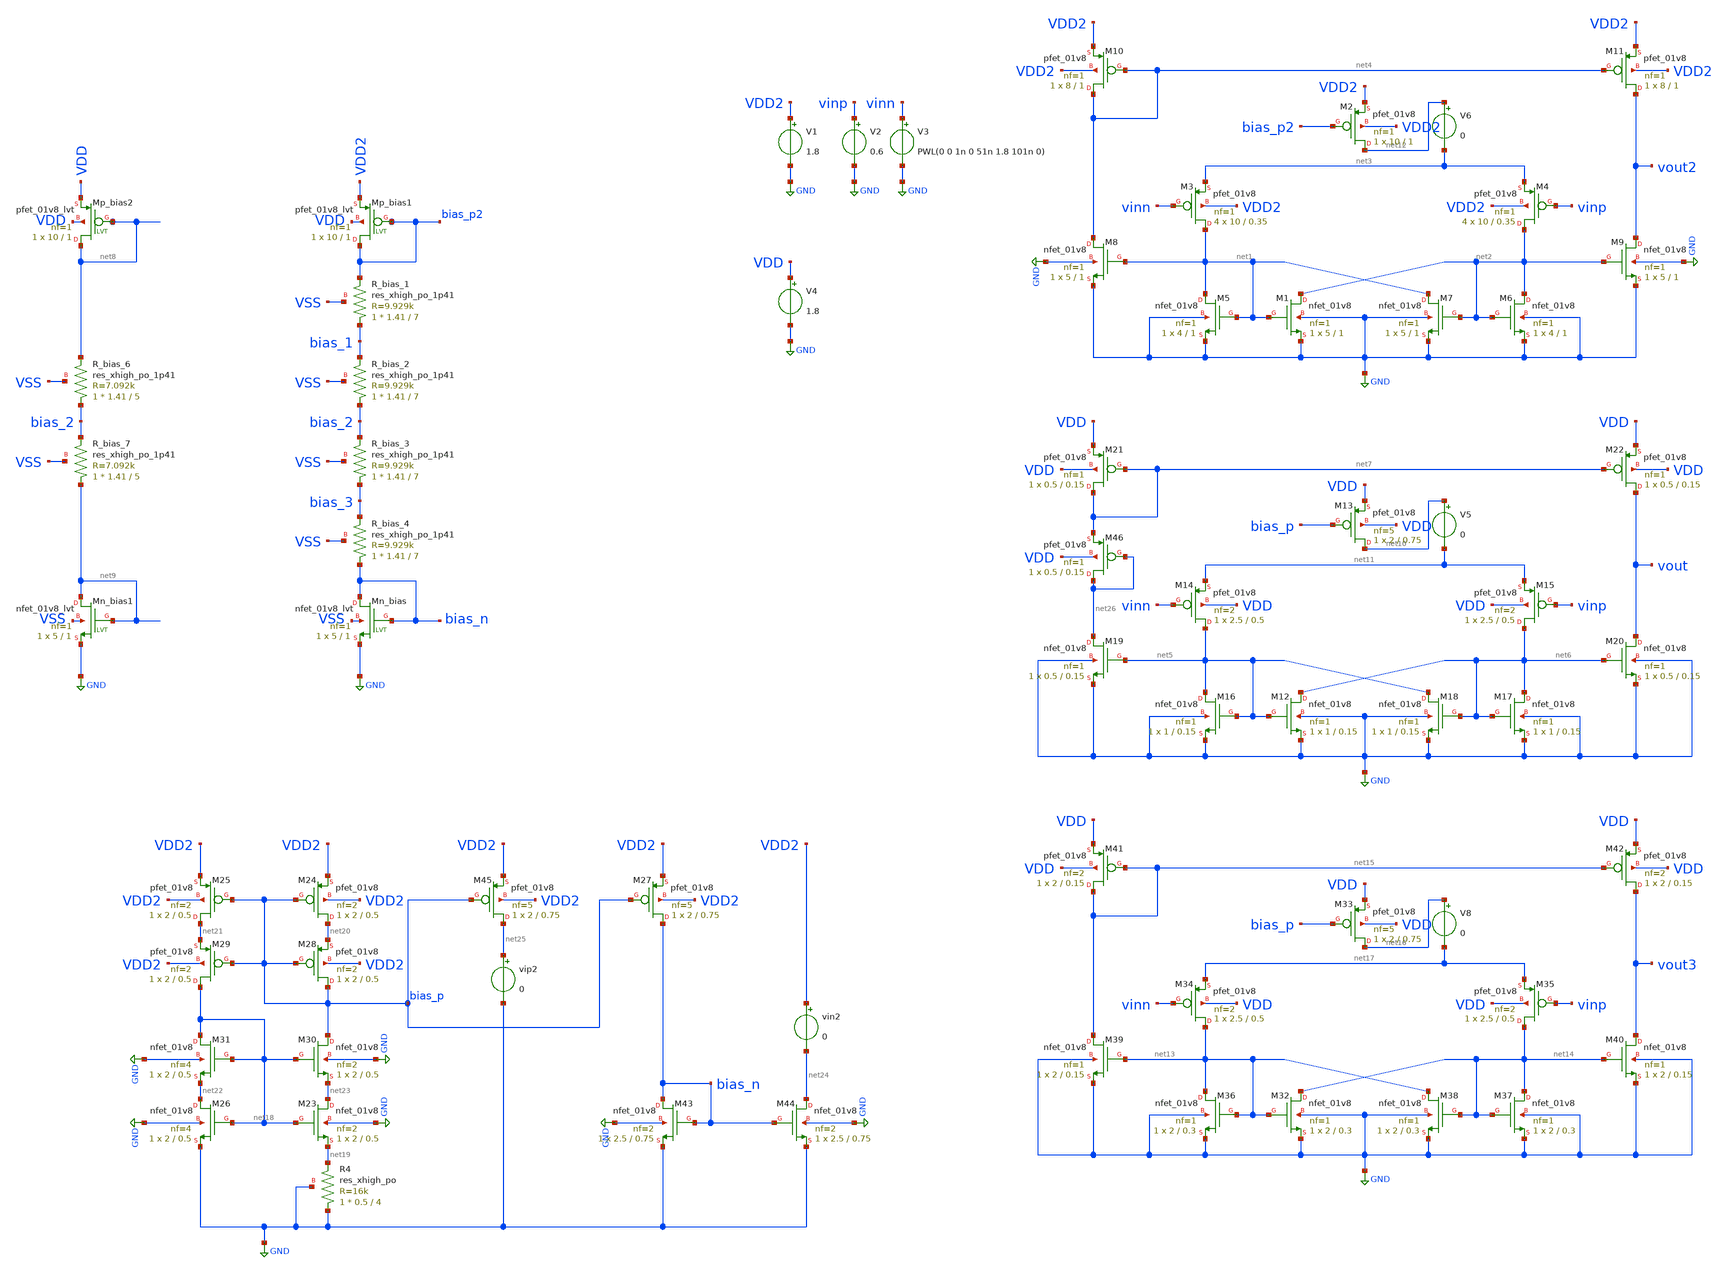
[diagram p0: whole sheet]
** sch_path: schem/comp_p.sch
**.subckt comp_p
XM1 net2 net1 GND GND sky130_fd_pr__nfet_01v8 L=1 W=5 nf=1 ad='int((1 + 1)/2) * 5 / 1 * 0.29' as='int((1 + 2)/2) * 5 / 1 * 0.29'
+ pd='2*int((1 + 1)/2) * (5 / 1 + 0.29)' ps='2*int((1 + 2)/2) * (5 / 1 + 0.29)' nrd='0.29 / 5 ' nrs='0.29 / 5 '
+ sa=0 sb=0 sd=0 mult=1 m=1
XM2 net12 bias_p2 VDD2 VDD2 sky130_fd_pr__pfet_01v8 L=1 W=10 nf=1 ad='int((1 + 1)/2) * 10 / 1 * 0.29'
+ as='int((1 + 2)/2) * 10 / 1 * 0.29' pd='2*int((1 + 1)/2) * (10 / 1 + 0.29)' ps='2*int((1 + 2)/2) * (10 / 1 + 0.29)'
+ nrd='0.29 / 10 ' nrs='0.29 / 10 ' sa=0 sb=0 sd=0 mult=1 m=1
XM3 net1 vinn net3 VDD2 sky130_fd_pr__pfet_01v8 L=0.35 W=10 nf=1 ad='int((1 + 1)/2) * 10 / 1 * 0.29'
+ as='int((1 + 2)/2) * 10 / 1 * 0.29' pd='2*int((1 + 1)/2) * (10 / 1 + 0.29)' ps='2*int((1 + 2)/2) * (10 / 1 + 0.29)'
+ nrd='0.29 / 10 ' nrs='0.29 / 10 ' sa=0 sb=0 sd=0 mult=4 m=4
XM4 net2 vinp net3 VDD2 sky130_fd_pr__pfet_01v8 L=0.35 W=10 nf=1 ad='int((1 + 1)/2) * 10 / 1 * 0.29'
+ as='int((1 + 2)/2) * 10 / 1 * 0.29' pd='2*int((1 + 1)/2) * (10 / 1 + 0.29)' ps='2*int((1 + 2)/2) * (10 / 1 + 0.29)'
+ nrd='0.29 / 10 ' nrs='0.29 / 10 ' sa=0 sb=0 sd=0 mult=4 m=4
XM5 net1 net1 GND GND sky130_fd_pr__nfet_01v8 L=1 W=4 nf=1 ad='int((1 + 1)/2) * 4 / 1 * 0.29' as='int((1 + 2)/2) * 4 / 1 * 0.29'
+ pd='2*int((1 + 1)/2) * (4 / 1 + 0.29)' ps='2*int((1 + 2)/2) * (4 / 1 + 0.29)' nrd='0.29 / 4 ' nrs='0.29 / 4 '
+ sa=0 sb=0 sd=0 mult=1 m=1
XM6 net2 net2 GND GND sky130_fd_pr__nfet_01v8 L=1 W=4 nf=1 ad='int((1 + 1)/2) * 4 / 1 * 0.29' as='int((1 + 2)/2) * 4 / 1 * 0.29'
+ pd='2*int((1 + 1)/2) * (4 / 1 + 0.29)' ps='2*int((1 + 2)/2) * (4 / 1 + 0.29)' nrd='0.29 / 4 ' nrs='0.29 / 4 '
+ sa=0 sb=0 sd=0 mult=1 m=1
XM7 net1 net2 GND GND sky130_fd_pr__nfet_01v8 L=1 W=5 nf=1 ad='int((1 + 1)/2) * 5 / 1 * 0.29' as='int((1 + 2)/2) * 5 / 1 * 0.29'
+ pd='2*int((1 + 1)/2) * (5 / 1 + 0.29)' ps='2*int((1 + 2)/2) * (5 / 1 + 0.29)' nrd='0.29 / 5 ' nrs='0.29 / 5 '
+ sa=0 sb=0 sd=0 mult=1 m=1
XM8 net4 net1 GND GND sky130_fd_pr__nfet_01v8 L=1 W=5 nf=1 ad='int((1 + 1)/2) * 5 / 1 * 0.29' as='int((1 + 2)/2) * 5 / 1 * 0.29'
+ pd='2*int((1 + 1)/2) * (5 / 1 + 0.29)' ps='2*int((1 + 2)/2) * (5 / 1 + 0.29)' nrd='0.29 / 5 ' nrs='0.29 / 5 '
+ sa=0 sb=0 sd=0 mult=1 m=1
XM9 vout2 net2 GND GND sky130_fd_pr__nfet_01v8 L=1 W=5 nf=1 ad='int((1 + 1)/2) * 5 / 1 * 0.29' as='int((1 + 2)/2) * 5 / 1 * 0.29'
+ pd='2*int((1 + 1)/2) * (5 / 1 + 0.29)' ps='2*int((1 + 2)/2) * (5 / 1 + 0.29)' nrd='0.29 / 5 ' nrs='0.29 / 5 '
+ sa=0 sb=0 sd=0 mult=1 m=1
XM10 net4 net4 VDD2 VDD2 sky130_fd_pr__pfet_01v8 L=1 W=8 nf=1 ad='int((1 + 1)/2) * 8 / 1 * 0.29' as='int((1 + 2)/2) * 8 / 1 * 0.29'
+ pd='2*int((1 + 1)/2) * (8 / 1 + 0.29)' ps='2*int((1 + 2)/2) * (8 / 1 + 0.29)' nrd='0.29 / 8 ' nrs='0.29 / 8 '
+ sa=0 sb=0 sd=0 mult=1 m=1
XM11 vout2 net4 VDD2 VDD2 sky130_fd_pr__pfet_01v8 L=1 W=8 nf=1 ad='int((1 + 1)/2) * 8 / 1 * 0.29' as='int((1 + 2)/2) * 8 / 1 * 0.29'
+ pd='2*int((1 + 1)/2) * (8 / 1 + 0.29)' ps='2*int((1 + 2)/2) * (8 / 1 + 0.29)' nrd='0.29 / 8 ' nrs='0.29 / 8 '
+ sa=0 sb=0 sd=0 mult=1 m=1
V1 VDD2 GND 1.8
V2 vinp GND 0.6
V3 vinn GND PWL(0 0 1n 0 51n 1.8 101n 0)
XR_bias_1 bias_1 bias_p2 VSS sky130_fd_pr__res_xhigh_po_1p41 L=7 mult=1 m=1
XMn_bias bias_n bias_n GND VSS sky130_fd_pr__nfet_01v8_lvt L=1 W=5 nf=1 ad='int((nf+1)/2) * W/nf * 0.29'
+ as='int((nf+2)/2) * W/nf * 0.29' pd='2*int((nf+1)/2) * (W/nf + 0.29)' ps='2*int((nf+2)/2) * (W/nf + 0.29)'
+ nrd='0.29 / W' nrs='0.29 / W' sa=0 sb=0 sd=0 mult=1 m=1
XMp_bias1 bias_p2 bias_p2 VDD2 VDD sky130_fd_pr__pfet_01v8_lvt L=1 W=10 nf=1 ad='int((nf+1)/2) * W/nf * 0.29'
+ as='int((nf+2)/2) * W/nf * 0.29' pd='2*int((nf+1)/2) * (W/nf + 0.29)' ps='2*int((nf+2)/2) * (W/nf + 0.29)'
+ nrd='0.29 / W' nrs='0.29 / W' sa=0 sb=0 sd=0 mult=1 m=1
XR_bias_2 bias_2 bias_1 VSS sky130_fd_pr__res_xhigh_po_1p41 L=7 mult=1 m=1
XR_bias_3 bias_3 bias_2 VSS sky130_fd_pr__res_xhigh_po_1p41 L=7 mult=1 m=1
XR_bias_4 bias_n bias_3 VSS sky130_fd_pr__res_xhigh_po_1p41 L=7 mult=1 m=1
XM12 net6 net5 GND GND sky130_fd_pr__nfet_01v8 L=0.15 W=1 nf=1 ad='int((1 + 1)/2) * 1 / 1 * 0.29' as='int((1 + 2)/2) * 1 / 1 * 0.29'
+ pd='2*int((1 + 1)/2) * (1 / 1 + 0.29)' ps='2*int((1 + 2)/2) * (1 / 1 + 0.29)' nrd='0.29 / 1 ' nrs='0.29 / 1 '
+ sa=0 sb=0 sd=0 mult=1 m=1
XM13 net10 bias_p VDD VDD sky130_fd_pr__pfet_01v8 L=0.75 W=2 nf=5 ad='int((5 + 1)/2) * 2 / 5 * 0.29'
+ as='int((5 + 2)/2) * 2 / 5 * 0.29' pd='2*int((5 + 1)/2) * (2 / 5 + 0.29)' ps='2*int((5 + 2)/2) * (2 / 5 + 0.29)'
+ nrd='0.29 / 2 ' nrs='0.29 / 2 ' sa=0 sb=0 sd=0 mult=1 m=1
XM14 net5 vinn net11 VDD sky130_fd_pr__pfet_01v8 L=0.5 W=2.5 nf=2 ad='int((2 + 1)/2) * 2.5 / 2 * 0.29'
+ as='int((2 + 2)/2) * 2.5 / 2 * 0.29' pd='2*int((2 + 1)/2) * (2.5 / 2 + 0.29)' ps='2*int((2 + 2)/2) * (2.5 / 2 + 0.29)'
+ nrd='0.29 / 2.5 ' nrs='0.29 / 2.5 ' sa=0 sb=0 sd=0 mult=1 m=1
XM15 net6 vinp net11 VDD sky130_fd_pr__pfet_01v8 L=0.5 W=2.5 nf=2 ad='int((2 + 1)/2) * 2.5 / 2 * 0.29'
+ as='int((2 + 2)/2) * 2.5 / 2 * 0.29' pd='2*int((2 + 1)/2) * (2.5 / 2 + 0.29)' ps='2*int((2 + 2)/2) * (2.5 / 2 + 0.29)'
+ nrd='0.29 / 2.5 ' nrs='0.29 / 2.5 ' sa=0 sb=0 sd=0 mult=1 m=1
XM16 net5 net5 GND GND sky130_fd_pr__nfet_01v8 L=0.15 W=1 nf=1 ad='int((1 + 1)/2) * 1 / 1 * 0.29' as='int((1 + 2)/2) * 1 / 1 * 0.29'
+ pd='2*int((1 + 1)/2) * (1 / 1 + 0.29)' ps='2*int((1 + 2)/2) * (1 / 1 + 0.29)' nrd='0.29 / 1 ' nrs='0.29 / 1 '
+ sa=0 sb=0 sd=0 mult=1 m=1
XM17 net6 net6 GND GND sky130_fd_pr__nfet_01v8 L=0.15 W=1 nf=1 ad='int((1 + 1)/2) * 1 / 1 * 0.29' as='int((1 + 2)/2) * 1 / 1 * 0.29'
+ pd='2*int((1 + 1)/2) * (1 / 1 + 0.29)' ps='2*int((1 + 2)/2) * (1 / 1 + 0.29)' nrd='0.29 / 1 ' nrs='0.29 / 1 '
+ sa=0 sb=0 sd=0 mult=1 m=1
XM18 net5 net6 GND GND sky130_fd_pr__nfet_01v8 L=0.15 W=1 nf=1 ad='int((1 + 1)/2) * 1 / 1 * 0.29' as='int((1 + 2)/2) * 1 / 1 * 0.29'
+ pd='2*int((1 + 1)/2) * (1 / 1 + 0.29)' ps='2*int((1 + 2)/2) * (1 / 1 + 0.29)' nrd='0.29 / 1 ' nrs='0.29 / 1 '
+ sa=0 sb=0 sd=0 mult=1 m=1
XM19 net26 net5 GND GND sky130_fd_pr__nfet_01v8 L=0.15 W=0.5 nf=1 ad='int((1 + 1)/2) * 0.5 / 1 * 0.29'
+ as='int((1 + 2)/2) * 0.5 / 1 * 0.29' pd='2*int((1 + 1)/2) * (0.5 / 1 + 0.29)' ps='2*int((1 + 2)/2) * (0.5 / 1 + 0.29)'
+ nrd='0.29 / 0.5 ' nrs='0.29 / 0.5 ' sa=0 sb=0 sd=0 mult=1 m=1
XM20 vout net6 GND GND sky130_fd_pr__nfet_01v8 L=0.15 W=0.5 nf=1 ad='int((1 + 1)/2) * 0.5 / 1 * 0.29'
+ as='int((1 + 2)/2) * 0.5 / 1 * 0.29' pd='2*int((1 + 1)/2) * (0.5 / 1 + 0.29)' ps='2*int((1 + 2)/2) * (0.5 / 1 + 0.29)'
+ nrd='0.29 / 0.5 ' nrs='0.29 / 0.5 ' sa=0 sb=0 sd=0 mult=1 m=1
XM21 net7 net7 VDD VDD sky130_fd_pr__pfet_01v8 L=0.15 W=0.5 nf=1 ad='int((1 + 1)/2) * 0.5 / 1 * 0.29'
+ as='int((1 + 2)/2) * 0.5 / 1 * 0.29' pd='2*int((1 + 1)/2) * (0.5 / 1 + 0.29)' ps='2*int((1 + 2)/2) * (0.5 / 1 + 0.29)'
+ nrd='0.29 / 0.5 ' nrs='0.29 / 0.5 ' sa=0 sb=0 sd=0 mult=1 m=1
XM22 vout net7 VDD VDD sky130_fd_pr__pfet_01v8 L=0.15 W=0.5 nf=1 ad='int((1 + 1)/2) * 0.5 / 1 * 0.29'
+ as='int((1 + 2)/2) * 0.5 / 1 * 0.29' pd='2*int((1 + 1)/2) * (0.5 / 1 + 0.29)' ps='2*int((1 + 2)/2) * (0.5 / 1 + 0.29)'
+ nrd='0.29 / 0.5 ' nrs='0.29 / 0.5 ' sa=0 sb=0 sd=0 mult=1 m=1
V4 VDD GND 1.8
XMn_bias1 net9 net9 GND VSS sky130_fd_pr__nfet_01v8_lvt L=1 W=5 nf=1 ad='int((nf+1)/2) * W/nf * 0.29'
+ as='int((nf+2)/2) * W/nf * 0.29' pd='2*int((nf+1)/2) * (W/nf + 0.29)' ps='2*int((nf+2)/2) * (W/nf + 0.29)'
+ nrd='0.29 / W' nrs='0.29 / W' sa=0 sb=0 sd=0 mult=1 m=1
XMp_bias2 net8 net8 VDD VDD sky130_fd_pr__pfet_01v8_lvt L=1 W=10 nf=1 ad='int((nf+1)/2) * W/nf * 0.29'
+ as='int((nf+2)/2) * W/nf * 0.29' pd='2*int((nf+1)/2) * (W/nf + 0.29)' ps='2*int((nf+2)/2) * (W/nf + 0.29)'
+ nrd='0.29 / W' nrs='0.29 / W' sa=0 sb=0 sd=0 mult=1 m=1
XR_bias_6 bias_2 net8 VSS sky130_fd_pr__res_xhigh_po_1p41 L=5 mult=1 m=1
XR_bias_7 net9 bias_2 VSS sky130_fd_pr__res_xhigh_po_1p41 L=5 mult=1 m=1
V5 net10 net11 0
.save i(v5)
V6 net12 net3 0
.save i(v6)
XM32 net14 net13 GND GND sky130_fd_pr__nfet_01v8 L=0.3 W=2 nf=1 ad='int((1 + 1)/2) * 2 / 1 * 0.29' as='int((1 + 2)/2) * 2 / 1 * 0.29'
+ pd='2*int((1 + 1)/2) * (2 / 1 + 0.29)' ps='2*int((1 + 2)/2) * (2 / 1 + 0.29)' nrd='0.29 / 2 ' nrs='0.29 / 2 '
+ sa=0 sb=0 sd=0 mult=1 m=1
XM33 net16 bias_p VDD VDD sky130_fd_pr__pfet_01v8 L=0.75 W=2 nf=5 ad='int((5 + 1)/2) * 2 / 5 * 0.29'
+ as='int((5 + 2)/2) * 2 / 5 * 0.29' pd='2*int((5 + 1)/2) * (2 / 5 + 0.29)' ps='2*int((5 + 2)/2) * (2 / 5 + 0.29)'
+ nrd='0.29 / 2 ' nrs='0.29 / 2 ' sa=0 sb=0 sd=0 mult=1 m=1
XM34 net13 vinn net17 VDD sky130_fd_pr__pfet_01v8 L=0.5 W=2.5 nf=2 ad='int((2 + 1)/2) * 2.5 / 2 * 0.29'
+ as='int((2 + 2)/2) * 2.5 / 2 * 0.29' pd='2*int((2 + 1)/2) * (2.5 / 2 + 0.29)' ps='2*int((2 + 2)/2) * (2.5 / 2 + 0.29)'
+ nrd='0.29 / 2.5 ' nrs='0.29 / 2.5 ' sa=0 sb=0 sd=0 mult=1 m=1
XM35 net14 vinp net17 VDD sky130_fd_pr__pfet_01v8 L=0.5 W=2.5 nf=2 ad='int((2 + 1)/2) * 2.5 / 2 * 0.29'
+ as='int((2 + 2)/2) * 2.5 / 2 * 0.29' pd='2*int((2 + 1)/2) * (2.5 / 2 + 0.29)' ps='2*int((2 + 2)/2) * (2.5 / 2 + 0.29)'
+ nrd='0.29 / 2.5 ' nrs='0.29 / 2.5 ' sa=0 sb=0 sd=0 mult=1 m=1
XM36 net13 net13 GND GND sky130_fd_pr__nfet_01v8 L=0.3 W=2 nf=1 ad='int((1 + 1)/2) * 2 / 1 * 0.29' as='int((1 + 2)/2) * 2 / 1 * 0.29'
+ pd='2*int((1 + 1)/2) * (2 / 1 + 0.29)' ps='2*int((1 + 2)/2) * (2 / 1 + 0.29)' nrd='0.29 / 2 ' nrs='0.29 / 2 '
+ sa=0 sb=0 sd=0 mult=1 m=1
XM37 net14 net14 GND GND sky130_fd_pr__nfet_01v8 L=0.3 W=2 nf=1 ad='int((1 + 1)/2) * 2 / 1 * 0.29' as='int((1 + 2)/2) * 2 / 1 * 0.29'
+ pd='2*int((1 + 1)/2) * (2 / 1 + 0.29)' ps='2*int((1 + 2)/2) * (2 / 1 + 0.29)' nrd='0.29 / 2 ' nrs='0.29 / 2 '
+ sa=0 sb=0 sd=0 mult=1 m=1
XM38 net13 net14 GND GND sky130_fd_pr__nfet_01v8 L=0.3 W=2 nf=1 ad='int((1 + 1)/2) * 2 / 1 * 0.29' as='int((1 + 2)/2) * 2 / 1 * 0.29'
+ pd='2*int((1 + 1)/2) * (2 / 1 + 0.29)' ps='2*int((1 + 2)/2) * (2 / 1 + 0.29)' nrd='0.29 / 2 ' nrs='0.29 / 2 '
+ sa=0 sb=0 sd=0 mult=1 m=1
XM39 net15 net13 GND GND sky130_fd_pr__nfet_01v8 L=0.15 W=2 nf=1 ad='int((1 + 1)/2) * 2 / 1 * 0.29' as='int((1 + 2)/2) * 2 / 1 * 0.29'
+ pd='2*int((1 + 1)/2) * (2 / 1 + 0.29)' ps='2*int((1 + 2)/2) * (2 / 1 + 0.29)' nrd='0.29 / 2 ' nrs='0.29 / 2 '
+ sa=0 sb=0 sd=0 mult=1 m=1
XM40 vout3 net14 GND GND sky130_fd_pr__nfet_01v8 L=0.15 W=2 nf=1 ad='int((1 + 1)/2) * 2 / 1 * 0.29' as='int((1 + 2)/2) * 2 / 1 * 0.29'
+ pd='2*int((1 + 1)/2) * (2 / 1 + 0.29)' ps='2*int((1 + 2)/2) * (2 / 1 + 0.29)' nrd='0.29 / 2 ' nrs='0.29 / 2 '
+ sa=0 sb=0 sd=0 mult=1 m=1
XM41 net15 net15 VDD VDD sky130_fd_pr__pfet_01v8 L=0.15 W=2 nf=2 ad='int((2 + 1)/2) * 2 / 2 * 0.29' as='int((2 + 2)/2) * 2 / 2 * 0.29'
+ pd='2*int((2 + 1)/2) * (2 / 2 + 0.29)' ps='2*int((2 + 2)/2) * (2 / 2 + 0.29)' nrd='0.29 / 2 ' nrs='0.29 / 2 '
+ sa=0 sb=0 sd=0 mult=1 m=1
XM42 vout3 net15 VDD VDD sky130_fd_pr__pfet_01v8 L=0.15 W=2 nf=2 ad='int((2 + 1)/2) * 2 / 2 * 0.29' as='int((2 + 2)/2) * 2 / 2 * 0.29'
+ pd='2*int((2 + 1)/2) * (2 / 2 + 0.29)' ps='2*int((2 + 2)/2) * (2 / 2 + 0.29)' nrd='0.29 / 2 ' nrs='0.29 / 2 '
+ sa=0 sb=0 sd=0 mult=1 m=1
V8 net16 net17 0
.save i(v8)
XM23 net23 net18 net19 GND sky130_fd_pr__nfet_01v8 L=0.5 W=2 nf=2 ad='int((2 + 1)/2) * 2 / 2 * 0.29'
+ as='int((2 + 2)/2) * 2 / 2 * 0.29' pd='2*int((2 + 1)/2) * (2 / 2 + 0.29)' ps='2*int((2 + 2)/2) * (2 / 2 + 0.29)'
+ nrd='0.29 / 2 ' nrs='0.29 / 2 ' sa=0 sb=0 sd=0 mult=1 m=1
XM24 net20 bias_p VDD2 VDD2 sky130_fd_pr__pfet_01v8 L=0.5 W=2 nf=2 ad='int((2 + 1)/2) * 2 / 2 * 0.29'
+ as='int((2 + 2)/2) * 2 / 2 * 0.29' pd='2*int((2 + 1)/2) * (2 / 2 + 0.29)' ps='2*int((2 + 2)/2) * (2 / 2 + 0.29)'
+ nrd='0.29 / 2 ' nrs='0.29 / 2 ' sa=0 sb=0 sd=0 mult=1 m=1
XM25 net21 bias_p VDD2 VDD2 sky130_fd_pr__pfet_01v8 L=0.5 W=2 nf=2 ad='int((2 + 1)/2) * 2 / 2 * 0.29'
+ as='int((2 + 2)/2) * 2 / 2 * 0.29' pd='2*int((2 + 1)/2) * (2 / 2 + 0.29)' ps='2*int((2 + 2)/2) * (2 / 2 + 0.29)'
+ nrd='0.29 / 2 ' nrs='0.29 / 2 ' sa=0 sb=0 sd=0 mult=1 m=1
XM26 net22 net18 GND GND sky130_fd_pr__nfet_01v8 L=0.5 W=2 nf=4 ad='int((4 + 1)/2) * 2 / 4 * 0.29' as='int((4 + 2)/2) * 2 / 4 * 0.29'
+ pd='2*int((4 + 1)/2) * (2 / 4 + 0.29)' ps='2*int((4 + 2)/2) * (2 / 4 + 0.29)' nrd='0.29 / 2 ' nrs='0.29 / 2 '
+ sa=0 sb=0 sd=0 mult=1 m=1
XR4 GND net19 GND sky130_fd_pr__res_xhigh_po W=0.5 L=4 mult=1 m=1
XM27 bias_n bias_p VDD2 VDD2 sky130_fd_pr__pfet_01v8 L=0.75 W=2 nf=5 ad='int((5 + 1)/2) * 2 / 5 * 0.29'
+ as='int((5 + 2)/2) * 2 / 5 * 0.29' pd='2*int((5 + 1)/2) * (2 / 5 + 0.29)' ps='2*int((5 + 2)/2) * (2 / 5 + 0.29)'
+ nrd='0.29 / 2 ' nrs='0.29 / 2 ' sa=0 sb=0 sd=0 mult=1 m=1
XM28 bias_p bias_p net20 VDD2 sky130_fd_pr__pfet_01v8 L=0.5 W=2 nf=2 ad='int((2 + 1)/2) * 2 / 2 * 0.29'
+ as='int((2 + 2)/2) * 2 / 2 * 0.29' pd='2*int((2 + 1)/2) * (2 / 2 + 0.29)' ps='2*int((2 + 2)/2) * (2 / 2 + 0.29)'
+ nrd='0.29 / 2 ' nrs='0.29 / 2 ' sa=0 sb=0 sd=0 mult=1 m=1
XM29 net18 bias_p net21 VDD2 sky130_fd_pr__pfet_01v8 L=0.5 W=2 nf=2 ad='int((2 + 1)/2) * 2 / 2 * 0.29'
+ as='int((2 + 2)/2) * 2 / 2 * 0.29' pd='2*int((2 + 1)/2) * (2 / 2 + 0.29)' ps='2*int((2 + 2)/2) * (2 / 2 + 0.29)'
+ nrd='0.29 / 2 ' nrs='0.29 / 2 ' sa=0 sb=0 sd=0 mult=1 m=1
XM30 bias_p net18 net23 GND sky130_fd_pr__nfet_01v8 L=0.5 W=2 nf=2 ad='int((2 + 1)/2) * 2 / 2 * 0.29'
+ as='int((2 + 2)/2) * 2 / 2 * 0.29' pd='2*int((2 + 1)/2) * (2 / 2 + 0.29)' ps='2*int((2 + 2)/2) * (2 / 2 + 0.29)'
+ nrd='0.29 / 2 ' nrs='0.29 / 2 ' sa=0 sb=0 sd=0 mult=1 m=1
XM31 net18 net18 net22 GND sky130_fd_pr__nfet_01v8 L=0.5 W=2 nf=4 ad='int((4 + 1)/2) * 2 / 4 * 0.29'
+ as='int((4 + 2)/2) * 2 / 4 * 0.29' pd='2*int((4 + 1)/2) * (2 / 4 + 0.29)' ps='2*int((4 + 2)/2) * (2 / 4 + 0.29)'
+ nrd='0.29 / 2 ' nrs='0.29 / 2 ' sa=0 sb=0 sd=0 mult=1 m=1
XM43 bias_n bias_n GND GND sky130_fd_pr__nfet_01v8 L=0.75 W=2.5 nf=2 ad='int((2 + 1)/2) * 2.5 / 2 * 0.29'
+ as='int((2 + 2)/2) * 2.5 / 2 * 0.29' pd='2*int((2 + 1)/2) * (2.5 / 2 + 0.29)' ps='2*int((2 + 2)/2) * (2.5 / 2 + 0.29)'
+ nrd='0.29 / 2.5 ' nrs='0.29 / 2.5 ' sa=0 sb=0 sd=0 mult=1 m=1
XM44 net24 bias_n GND GND sky130_fd_pr__nfet_01v8 L=0.75 W=2.5 nf=2 ad='int((2 + 1)/2) * 2.5 / 2 * 0.29'
+ as='int((2 + 2)/2) * 2.5 / 2 * 0.29' pd='2*int((2 + 1)/2) * (2.5 / 2 + 0.29)' ps='2*int((2 + 2)/2) * (2.5 / 2 + 0.29)'
+ nrd='0.29 / 2.5 ' nrs='0.29 / 2.5 ' sa=0 sb=0 sd=0 mult=1 m=1
vin2 VDD2 net24 0
XM45 net25 bias_p VDD2 VDD2 sky130_fd_pr__pfet_01v8 L=0.75 W=2 nf=5 ad='int((5 + 1)/2) * 2 / 5 * 0.29'
+ as='int((5 + 2)/2) * 2 / 5 * 0.29' pd='2*int((5 + 1)/2) * (2 / 5 + 0.29)' ps='2*int((5 + 2)/2) * (2 / 5 + 0.29)'
+ nrd='0.29 / 2 ' nrs='0.29 / 2 ' sa=0 sb=0 sd=0 mult=1 m=1
vip2 net25 GND 0
XM46 net26 net26 net7 VDD sky130_fd_pr__pfet_01v8 L=0.15 W=0.5 nf=1 ad='int((1 + 1)/2) * 0.5 / 1 * 0.29'
+ as='int((1 + 2)/2) * 0.5 / 1 * 0.29' pd='2*int((1 + 1)/2) * (0.5 / 1 + 0.29)' ps='2*int((1 + 2)/2) * (0.5 / 1 + 0.29)'
+ nrd='0.29 / 0.5 ' nrs='0.29 / 0.5 ' sa=0 sb=0 sd=0 mult=1 m=1
**** begin user architecture code


.lib /usr/local/share/pdk/sky130A/libs.tech/ngspice/sky130.lib.spice tt

.tran 0.01n 101n
.save all

.control
    run
    plot vinn vinp vout3 vout4
    plot abs(i(v5)) abs(i(v8))
.endc

.end


**** end user architecture code
**.ends
.GLOBAL GND
.end
